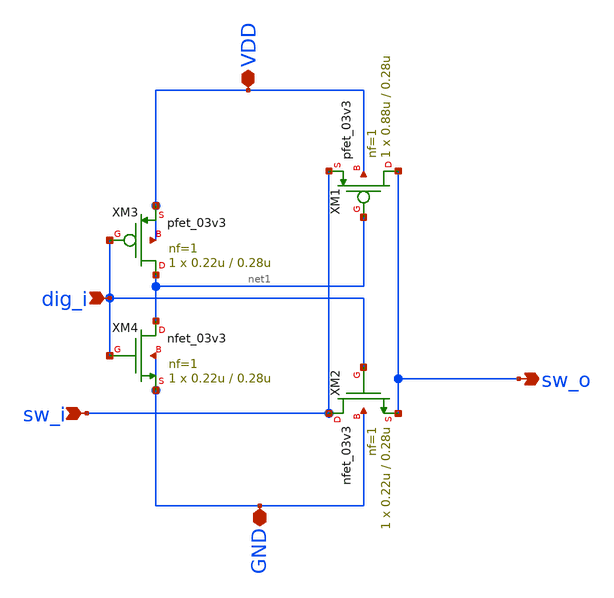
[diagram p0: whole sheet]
** sch_path: analog/B04_switch.sch
**.subckt B04_switch VDD GND sw_i sw_o dig_i
*.iopin VDD
*.iopin GND
*.ipin sw_i
*.opin sw_o
*.ipin dig_i
XM1 sw_o net1 sw_i VDD pfet_03v3 L=0.28u W=0.88u nf=1 ad='int((nf+1)/2) * W/nf * 0.18u' as='int((nf+2)/2) * W/nf * 0.18u'
+ pd='2*int((nf+1)/2) * (W/nf + 0.18u)' ps='2*int((nf+2)/2) * (W/nf + 0.18u)' nrd='0.18u / W' nrs='0.18u / W'
+ sa=0 sb=0 sd=0 m=1
XM2 sw_i dig_i sw_o GND nfet_03v3 L=0.28u W=0.22u nf=1 ad='int((nf+1)/2) * W/nf * 0.18u' as='int((nf+2)/2) * W/nf * 0.18u'
+ pd='2*int((nf+1)/2) * (W/nf + 0.18u)' ps='2*int((nf+2)/2) * (W/nf + 0.18u)' nrd='0.18u / W' nrs='0.18u / W'
+ sa=0 sb=0 sd=0 m=1
XM3 net1 dig_i VDD VDD pfet_03v3 L=0.28u W=0.22u nf=1 ad='int((nf+1)/2) * W/nf * 0.18u' as='int((nf+2)/2) * W/nf * 0.18u'
+ pd='2*int((nf+1)/2) * (W/nf + 0.18u)' ps='2*int((nf+2)/2) * (W/nf + 0.18u)' nrd='0.18u / W' nrs='0.18u / W'
+ sa=0 sb=0 sd=0 m=1
XM4 net1 dig_i GND GND nfet_03v3 L=0.28u W=0.22u nf=1 ad='int((nf+1)/2) * W/nf * 0.18u' as='int((nf+2)/2) * W/nf * 0.18u'
+ pd='2*int((nf+1)/2) * (W/nf + 0.18u)' ps='2*int((nf+2)/2) * (W/nf + 0.18u)' nrd='0.18u / W' nrs='0.18u / W'
+ sa=0 sb=0 sd=0 m=1
**.ends
.end
